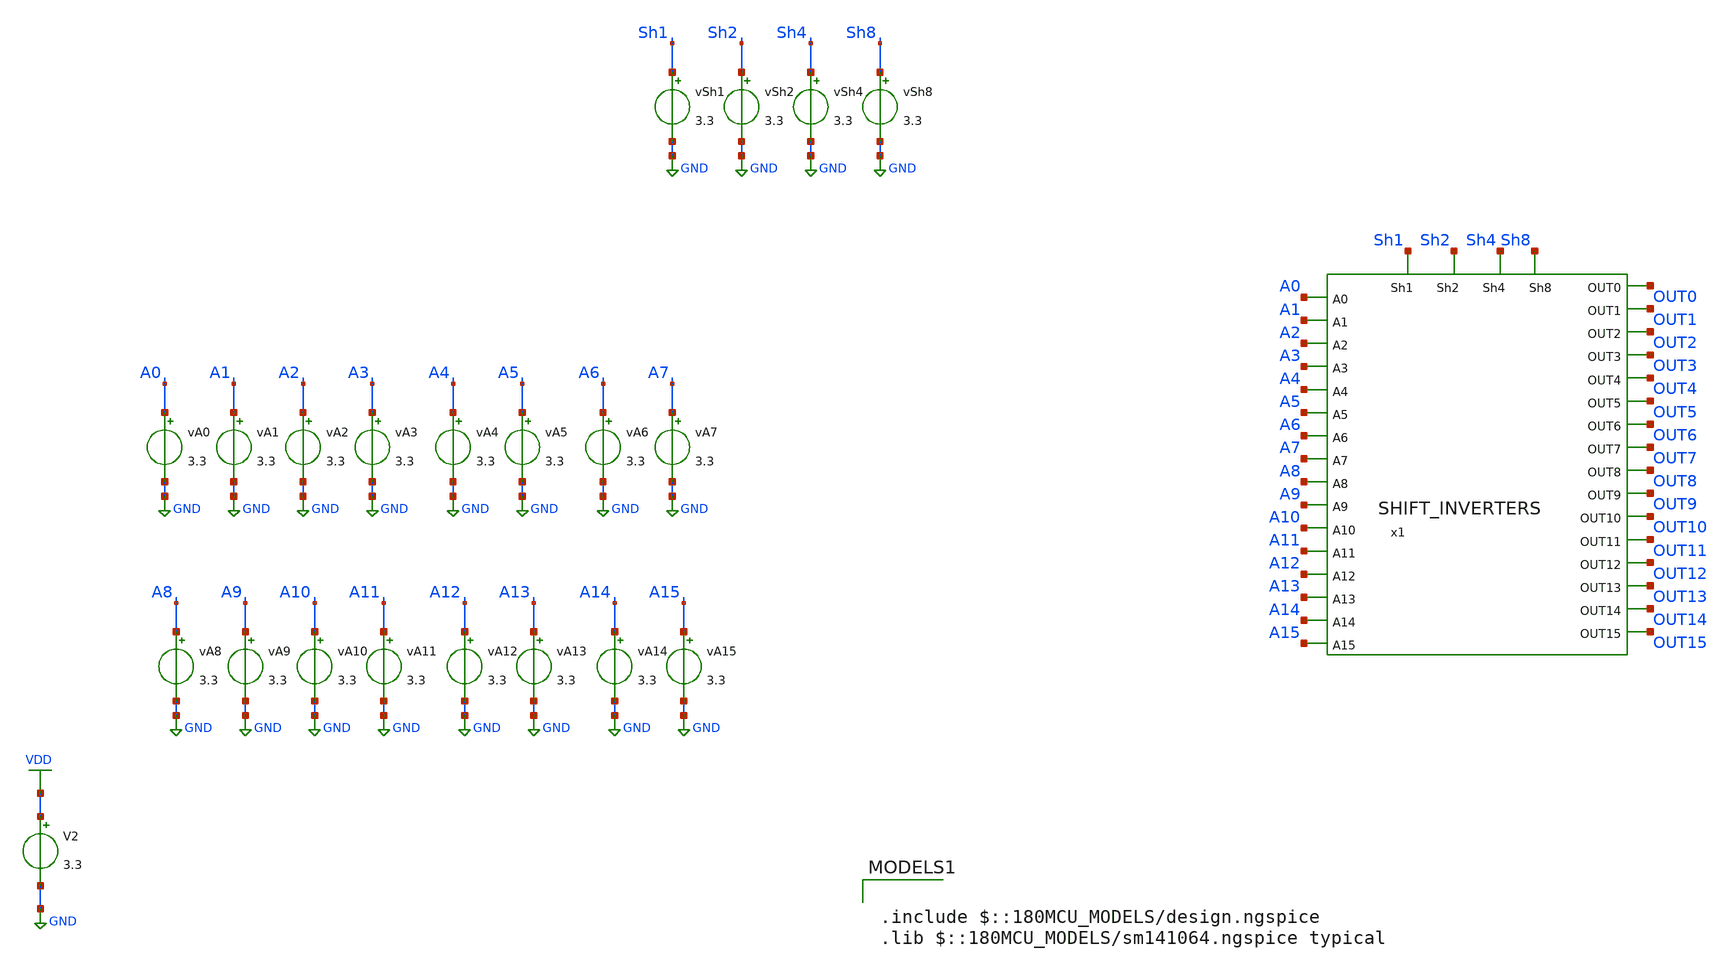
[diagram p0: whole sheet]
** sch_path: tbs/shift_tb_14_and_15.sch
**.subckt shift_tb_14_and_15
x1 OUT0 Sh1 OUT1 OUT2 Sh2 OUT3 OUT4 A0 OUT5 A1 OUT6 Sh4 OUT7 OUT8 A2 A3 OUT9 OUT10 OUT11 Sh8 OUT12
+ A4 OUT13 A5 A6 OUT14 A7 OUT15 A8 A9 A10 A11 A12 A13 A14 A15 SHIFT_INVERTERS
vA0 A0 GND 3.3
vA1 A1 GND 3.3
vA2 A2 GND 3.3
vA3 A3 GND 3.3
vA4 A4 GND 3.3
vA5 A5 GND 3.3
vA6 A6 GND 3.3
vA7 A7 GND 3.3
vA8 A8 GND 3.3
vA9 A9 GND 3.3
vA10 A10 GND 3.3
vA11 A11 GND 3.3
vA12 A12 GND 3.3
vA13 A13 GND 3.3
vA14 A14 GND 3.3
vA15 A15 GND 3.3
vSh1 Sh1 GND 3.3
vSh2 Sh2 GND 3.3
vSh4 Sh4 GND 3.3
vSh8 Sh8 GND 3.3
V2 VDD GND 3.3
**** begin user architecture code

.include $::180MCU_MODELS/design.ngspice
.lib $::180MCU_MODELS/sm141064.ngspice typical



.control
let vlow = 0
let vhigh = 3.3
* A = 1010101010101010 = 43690
alter VA15 = $&vhigh
alter VA14 = $&vlow
alter VA13 = $&vhigh
alter VA12 = $&vlow
alter VA11 = $&vhigh
alter VA10 = $&vlow
alter VA9  = $&vhigh
alter VA8  = $&vlow
alter VA7  = $&vhigh
alter VA6  = $&vlow
alter VA5  = $&vhigh
alter VA4  = $&vlow
alter VA3  = $&vhigh
alter VA2  = $&vlow
alter VA1  = $&vhigh
alter VA0  = $&vlow


* --- SHIFT 14 (1110) ---
alter vSh1 = $&vlow
alter vSh2 = $&vhigh
tran 1n 40n

meas tran v14_0  find v(OUT0)  at=30n
meas tran v14_1  find v(OUT1)  at=30n
meas tran v14_2  find v(OUT2)  at=30n
meas tran v14_3  find v(OUT3)  at=30n
meas tran v14_4  find v(OUT4)  at=30n
meas tran v14_5  find v(OUT5)  at=30n
meas tran v14_6  find v(OUT6)  at=30n
meas tran v14_7  find v(OUT7)  at=30n
meas tran v14_8  find v(OUT8)  at=30n
meas tran v14_9  find v(OUT9)  at=30n
meas tran v14_10 find v(OUT10) at=30n
meas tran v14_11 find v(OUT11) at=30n
meas tran v14_12 find v(OUT12) at=30n
meas tran v14_13 find v(OUT13) at=30n
meas tran v14_14 find v(OUT14) at=30n
meas tran v14_15 find v(OUT15) at=30n

let res14 = 0
if v14_0 > 1.6
  let res14 = res14 + 1
end
if v14_1 > 1.6
  let res14 = res14 + 2
end
if v14_2 > 1.6
  let res14 = res14 + 4
end
if v14_3 > 1.6
  let res14 = res14 + 8
end
if v14_4 > 1.6
  let res14 = res14 + 16
end
if v14_5 > 1.6
  let res14 = res14 + 32
end
if v14_6 > 1.6
  let res14 = res14 + 64
end
if v14_7 > 1.6
  let res14 = res14 + 128
end
if v14_8 > 1.6
  let res14 = res14 + 256
end
if v14_9 > 1.6
  let res14 = res14 + 512
end
if v14_10 > 1.6
  let res14 = res14 + 1024
end
if v14_11 > 1.6
  let res14 = res14 + 2048
end
if v14_12 > 1.6
  let res14 = res14 + 4096
end
if v14_13 > 1.6
  let res14 = res14 + 8192
end
if v14_14 > 1.6
  let res14 = res14 + 16384
end
if v14_15 > 1.6
  let res14 = res14 + 32768
end
echo 14_gives_32768
print res14

* --- SHIFT 15 (1111) ---
alter vSh1 = $&vhigh
tran 1n 40n

meas tran v15_0  find v(OUT0)  at=30n
meas tran v15_1  find v(OUT1)  at=30n
meas tran v15_2  find v(OUT2)  at=30n
meas tran v15_3  find v(OUT3)  at=30n
meas tran v15_4  find v(OUT4)  at=30n
meas tran v15_5  find v(OUT5)  at=30n
meas tran v15_6  find v(OUT6)  at=30n
meas tran v15_7  find v(OUT7)  at=30n
meas tran v15_8  find v(OUT8)  at=30n
meas tran v15_9  find v(OUT9)  at=30n
meas tran v15_10 find v(OUT10) at=30n
meas tran v15_11 find v(OUT11) at=30n
meas tran v15_12 find v(OUT12) at=30n
meas tran v15_13 find v(OUT13) at=30n
meas tran v15_14 find v(OUT14) at=30n
meas tran v15_15 find v(OUT15) at=30n

let res15 = 0
if v15_0 > 1.6
  let res15 = res15 + 1
end
if v15_1 > 1.6
  let res15 = res15 + 2
end
if v15_2 > 1.6
  let res15 = res15 + 4
end
if v15_3 > 1.6
  let res15 = res15 + 8
end
if v15_4 > 1.6
  let res15 = res15 + 16
end
if v15_5 > 1.6
  let res15 = res15 + 32
end
if v15_6 > 1.6
  let res15 = res15 + 64
end
if v15_7 > 1.6
  let res15 = res15 + 128
end
if v15_8 > 1.6
  let res15 = res15 + 256
end
if v15_9 > 1.6
  let res15 = res15 + 512
end
if v15_10 > 1.6
  let res15 = res15 + 1024
end
if v15_11 > 1.6
  let res15 = res15 + 2048
end
if v15_12 > 1.6
  let res15 = res15 + 4096
end
if v15_13 > 1.6
  let res15 = res15 + 8192
end
if v15_14 > 1.6
  let res15 = res15 + 16384
end
if v15_15 > 1.6
  let res15 = res15 + 32768
end
echo 15_gives_0
print res15
.endc


**** end user architecture code
**.ends
.GLOBAL GND
.GLOBAL VDD
.end
